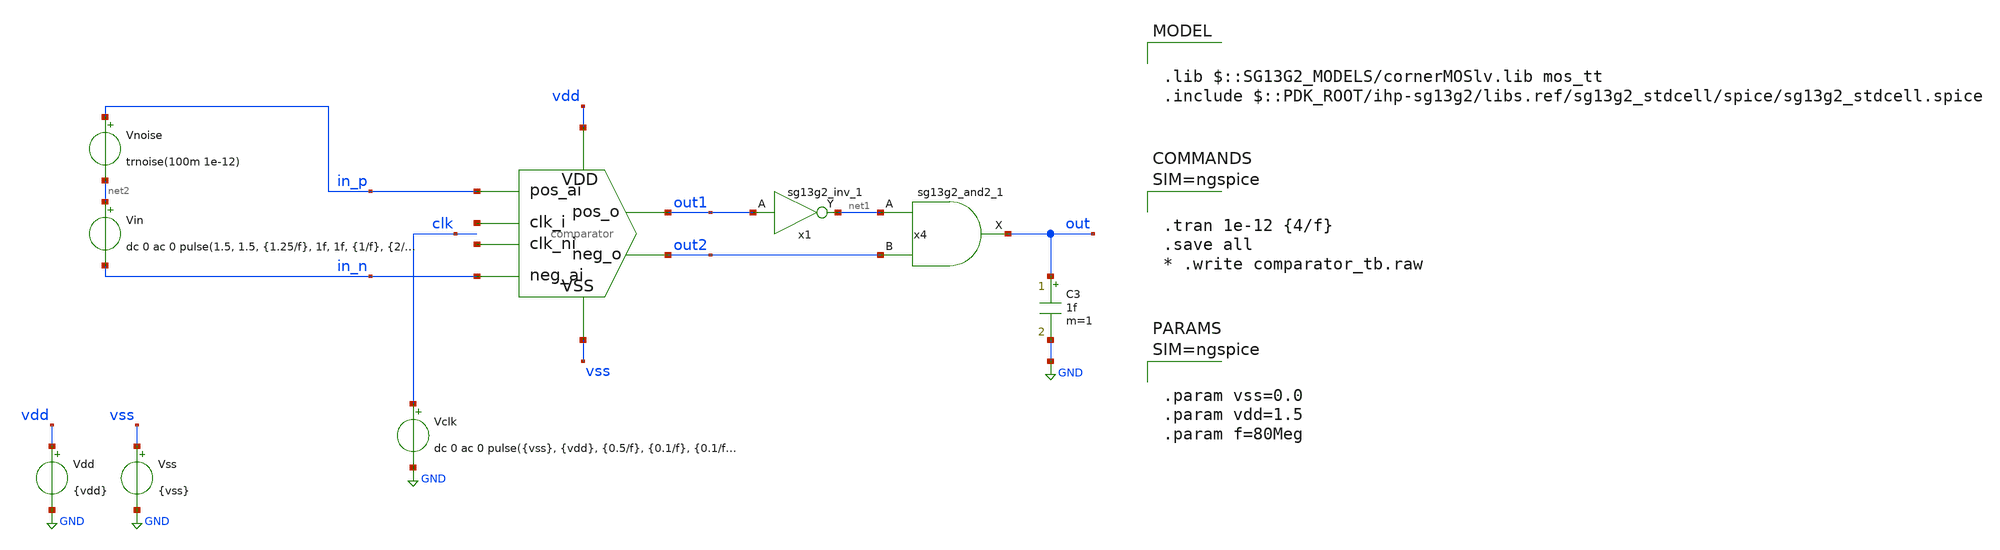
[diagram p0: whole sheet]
** sch_path: designs/comparator/comparator_tb.sch
**.subckt comparator_tb
x1 net3 in_p in_n out2 out1 vss vdd net4 comparator
Vdd vdd GND {vdd}
Vss vss GND {vss}
Vclk clk GND dc 0 ac 0 pulse({vss}, {vdd}, {0.5/f}, {0.1/f}, {0.1/f}, {0.4/f}, {1/f})
Vin net2 in_n dc 0 ac 0 pulse(1.5, 1.5, {1.25/f}, 1f, 1f, {1/f}, {2/f})
x1 net1 out1 VDD VSS sg13g2_inv_1
x4 out net1 out2 VDD VSS sg13g2_and2_1
C3 out GND 1f m=1
Vnoise in_p net2 trnoise(100m 1e-12)
**** begin user architecture code

.lib $::SG13G2_MODELS/cornerMOSlv.lib mos_tt
.include $::PDK_ROOT/ihp-sg13g2/libs.ref/sg13g2_stdcell/spice/sg13g2_stdcell.spice




.tran 1e-12 {4/f}
.save all
* .write comparator_tb.raw






.param vss=0.0
.param vdd=1.5
.param f=80Meg



**** end user architecture code
**.ends

* expanding   symbol:  comparator.sym # of pins=8
** sym_path: designs/comparator_dt/comparator.sym
** sch_path: designs/comparator_dt/comparator.sch
.subckt comparator clk_i pos_ai neg_ai neg_o pos_o VSS VDD clk_ni
*.ipin pos_ai
*.ipin neg_ai
*.ipin VSS
*.ipin VDD
*.opin neg_o
*.opin pos_o
*.ipin clk_i
*.ipin clk_ni
XM12 neg_buf clk_i VDD VDD sg13_lv_pmos w=1.0u l=0.13u ng=1 m=1 mm_ok=1
XM13 pos_buf clk_i VDD VDD sg13_lv_pmos w=1.0u l=0.13u ng=1 m=1 mm_ok=1
XM14 net1 pos_ai neg_buf VSS sg13_lv_nmos w=1.0u l=0.13u ng=1 m=1 mm_ok=1
XM15 net1 neg_ai pos_buf VSS sg13_lv_nmos w=1.0u l=0.13u ng=1 m=1 mm_ok=1
XM16 VSS clk_i net1 VSS sg13_lv_nmos w=1.0u l=0.13u ng=1 m=1 mm_ok=1
XM17 net2 clk_ni VDD VDD sg13_lv_pmos w=2.0u l=0.13u ng=2 m=1 mm_ok=1
XM18 pos_o neg_o net2 VDD sg13_lv_pmos w=2.0u l=0.13u ng=2 m=1 mm_ok=1
XM19 neg_o pos_o net2 VDD sg13_lv_pmos w=2.0u l=0.13u ng=2 m=1 mm_ok=1
XM20 VSS neg_buf pos_o VSS sg13_lv_nmos w=1.0u l=0.13u ng=1 m=1 mm_ok=1
XM21 VSS neg_o pos_o VSS sg13_lv_nmos w=1.0u l=0.13u ng=1 m=1 mm_ok=1
XM22 VSS pos_o neg_o VSS sg13_lv_nmos w=1.0u l=0.13u ng=1 m=1 mm_ok=1
XM23 VSS pos_buf neg_o VSS sg13_lv_nmos w=1.0u l=0.13u ng=1 m=1 mm_ok=1
XC1 neg_buf VSS cap_cmim w=1.41e-5 l=1.41e-5 m=1 mm_ok=1
XC2 pos_buf VSS cap_cmim w=1.41e-5 l=1.41e-5 m=1 mm_ok=1
.ends


* expanding   symbol:  sg13g2_stdcells/sg13g2_inv_1.sym # of pins=2
** sym_path: sg13g2_stdcells/sg13g2_inv_1.sym
** sch_path: sg13g2_stdcells/sg13g2_inv_1.sch
.subckt sg13g2_inv_1 Y A VDD VSS
*.opin Y
*.ipin A
*.iopin VDD
*.iopin VSS
XM1 Y A VSS VSS sg13_lv_nmos w=740.00n l=130.00n ng=1 m=1 mm_ok=1
XM2 Y A VDD VDD sg13_lv_pmos w=1.12u l=130.00n ng=1 m=1 mm_ok=1
.ends


* expanding   symbol:  sg13g2_stdcells/sg13g2_and2_1.sym # of pins=3
** sym_path: sg13g2_stdcells/sg13g2_and2_1.sym
** sch_path: sg13g2_stdcells/sg13g2_and2_1.sch
.subckt sg13g2_and2_1 X A B VDD VSS
*.ipin A
*.ipin B
*.opin X
*.iopin VDD
*.iopin VSS
XM1 net1 A net2 VSS sg13_lv_nmos w=640.00n l=130.00n ng=1 m=1 mm_ok=1
XM2 net2 B VSS VSS sg13_lv_nmos w=640.00n l=130.00n ng=1 m=1 mm_ok=1
XM3 X net1 VSS VSS sg13_lv_nmos w=740.00n l=130.00n ng=1 m=1 mm_ok=1
XM4 net1 B VDD VDD sg13_lv_pmos w=840.00n l=130.00n ng=1 m=1 mm_ok=1
XM5 net1 A VDD VDD sg13_lv_pmos w=840.00n l=130.00n ng=1 m=1 mm_ok=1
XM6 X net1 VDD VDD sg13_lv_pmos w=1.12u l=130.00n ng=1 m=1 mm_ok=1
.ends

.GLOBAL GND
.end
